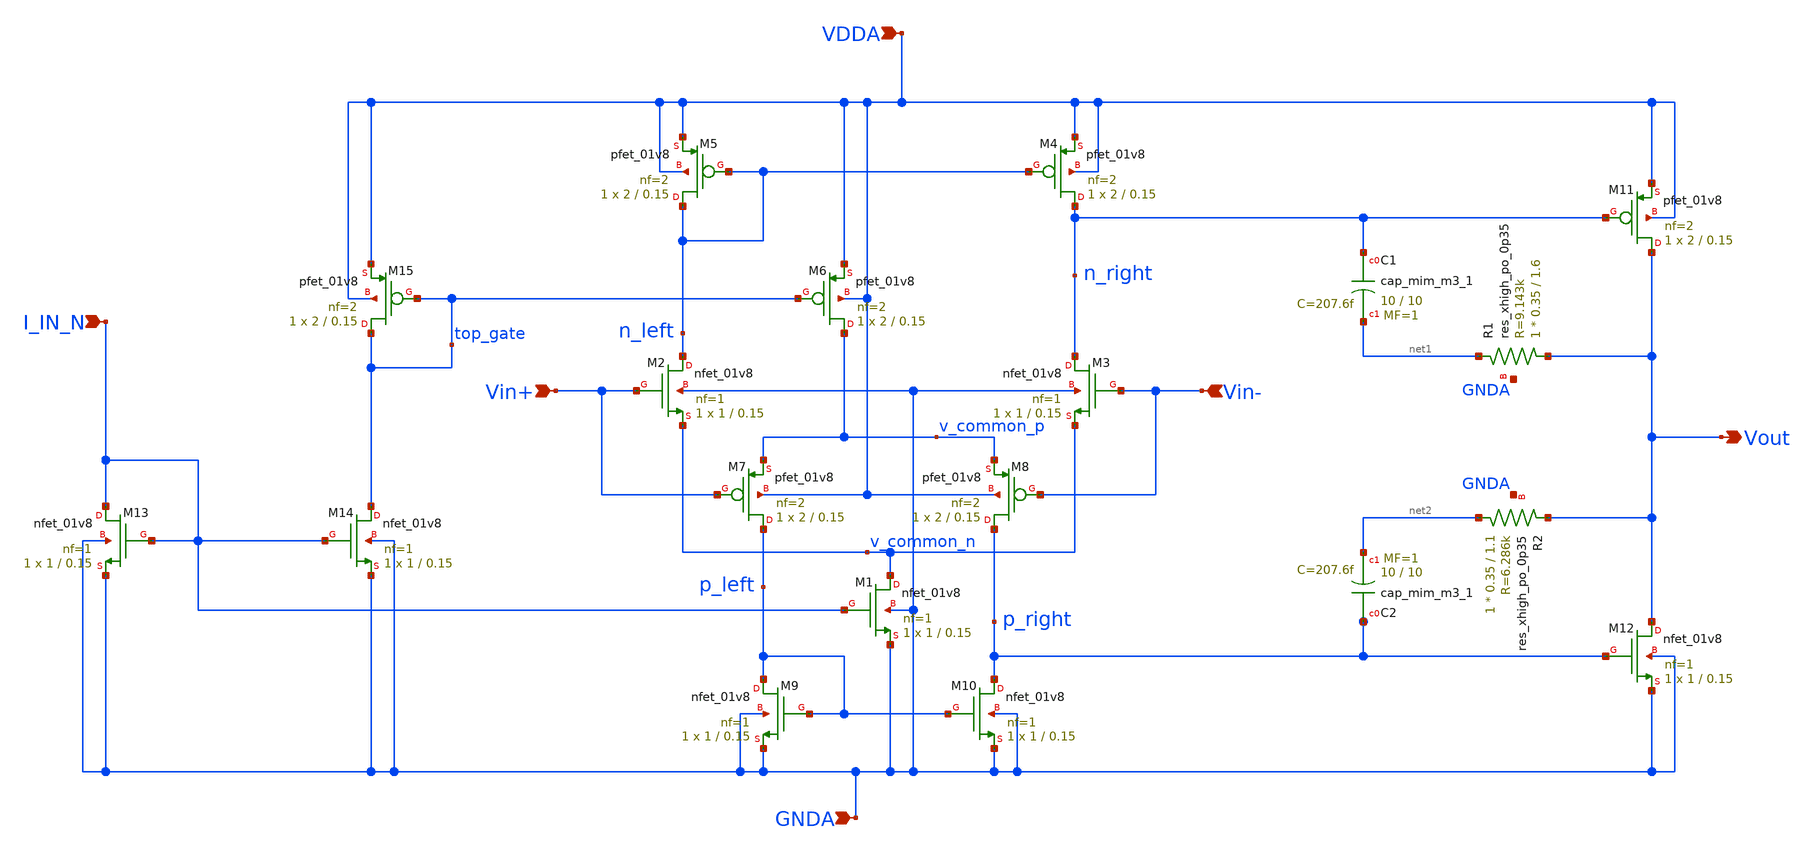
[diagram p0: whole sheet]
** sch_path: projects/pll/charge_pump/xschem_ngspice/rail_to_rail_opamp7.sch
**.subckt rail_to_rail_opamp7 Vout Vin+ Vin- VDDA GNDA I_IN_N
*.opin Vout
*.ipin Vin+
*.ipin Vin-
*.ipin VDDA
*.ipin GNDA
*.ipin I_IN_N
XM2 n_left Vin+ v_common_n GNDA sky130_fd_pr__nfet_01v8 L=0.15 W=1 nf=1 ad='int((nf+1)/2) * W/nf * 0.29'
+ as='int((nf+2)/2) * W/nf * 0.29' pd='2*int((nf+1)/2) * (W/nf + 0.29)' ps='2*int((nf+2)/2) * (W/nf + 0.29)'
+ nrd='0.29 / W' nrs='0.29 / W' sa=0 sb=0 sd=0 mult=1 m=1
XM3 n_right Vin- v_common_n GNDA sky130_fd_pr__nfet_01v8 L=0.15 W=1 nf=1 ad='int((nf+1)/2) * W/nf * 0.29'
+ as='int((nf+2)/2) * W/nf * 0.29' pd='2*int((nf+1)/2) * (W/nf + 0.29)' ps='2*int((nf+2)/2) * (W/nf + 0.29)'
+ nrd='0.29 / W' nrs='0.29 / W' sa=0 sb=0 sd=0 mult=1 m=1
XM5 n_left n_left VDDA VDDA sky130_fd_pr__pfet_01v8 L=0.15 W=2 nf=2 ad='int((nf+1)/2) * W/nf * 0.29'
+ as='int((nf+2)/2) * W/nf * 0.29' pd='2*int((nf+1)/2) * (W/nf + 0.29)' ps='2*int((nf+2)/2) * (W/nf + 0.29)'
+ nrd='0.29 / W' nrs='0.29 / W' sa=0 sb=0 sd=0 mult=1 m=1
XM4 n_right n_left VDDA VDDA sky130_fd_pr__pfet_01v8 L=0.15 W=2 nf=2 ad='int((nf+1)/2) * W/nf * 0.29'
+ as='int((nf+2)/2) * W/nf * 0.29' pd='2*int((nf+1)/2) * (W/nf + 0.29)' ps='2*int((nf+2)/2) * (W/nf + 0.29)'
+ nrd='0.29 / W' nrs='0.29 / W' sa=0 sb=0 sd=0 mult=1 m=1
XM6 v_common_p top_gate VDDA VDDA sky130_fd_pr__pfet_01v8 L=0.15 W=2 nf=2 ad='int((nf+1)/2) * W/nf * 0.29'
+ as='int((nf+2)/2) * W/nf * 0.29' pd='2*int((nf+1)/2) * (W/nf + 0.29)' ps='2*int((nf+2)/2) * (W/nf + 0.29)'
+ nrd='0.29 / W' nrs='0.29 / W' sa=0 sb=0 sd=0 mult=1 m=1
XM7 p_left Vin+ v_common_p VDDA sky130_fd_pr__pfet_01v8 L=0.15 W=2 nf=2 ad='int((nf+1)/2) * W/nf * 0.29'
+ as='int((nf+2)/2) * W/nf * 0.29' pd='2*int((nf+1)/2) * (W/nf + 0.29)' ps='2*int((nf+2)/2) * (W/nf + 0.29)'
+ nrd='0.29 / W' nrs='0.29 / W' sa=0 sb=0 sd=0 mult=1 m=1
XM8 p_right Vin- v_common_p VDDA sky130_fd_pr__pfet_01v8 L=0.15 W=2 nf=2 ad='int((nf+1)/2) * W/nf * 0.29'
+ as='int((nf+2)/2) * W/nf * 0.29' pd='2*int((nf+1)/2) * (W/nf + 0.29)' ps='2*int((nf+2)/2) * (W/nf + 0.29)'
+ nrd='0.29 / W' nrs='0.29 / W' sa=0 sb=0 sd=0 mult=1 m=1
XM9 p_left p_left GNDA GNDA sky130_fd_pr__nfet_01v8 L=0.15 W=1 nf=1 ad='int((nf+1)/2) * W/nf * 0.29'
+ as='int((nf+2)/2) * W/nf * 0.29' pd='2*int((nf+1)/2) * (W/nf + 0.29)' ps='2*int((nf+2)/2) * (W/nf + 0.29)'
+ nrd='0.29 / W' nrs='0.29 / W' sa=0 sb=0 sd=0 mult=1 m=1
XM10 p_right p_left GNDA GNDA sky130_fd_pr__nfet_01v8 L=0.15 W=1 nf=1 ad='int((nf+1)/2) * W/nf * 0.29'
+ as='int((nf+2)/2) * W/nf * 0.29' pd='2*int((nf+1)/2) * (W/nf + 0.29)' ps='2*int((nf+2)/2) * (W/nf + 0.29)'
+ nrd='0.29 / W' nrs='0.29 / W' sa=0 sb=0 sd=0 mult=1 m=1
XM1 v_common_n I_IN_N GNDA GNDA sky130_fd_pr__nfet_01v8 L=0.15 W=1 nf=1 ad='int((nf+1)/2) * W/nf * 0.29'
+ as='int((nf+2)/2) * W/nf * 0.29' pd='2*int((nf+1)/2) * (W/nf + 0.29)' ps='2*int((nf+2)/2) * (W/nf + 0.29)'
+ nrd='0.29 / W' nrs='0.29 / W' sa=0 sb=0 sd=0 mult=1 m=1
XM11 Vout n_right VDDA VDDA sky130_fd_pr__pfet_01v8 L=0.15 W=2 nf=2 ad='int((nf+1)/2) * W/nf * 0.29'
+ as='int((nf+2)/2) * W/nf * 0.29' pd='2*int((nf+1)/2) * (W/nf + 0.29)' ps='2*int((nf+2)/2) * (W/nf + 0.29)'
+ nrd='0.29 / W' nrs='0.29 / W' sa=0 sb=0 sd=0 mult=1 m=1
XM12 Vout p_right GNDA GNDA sky130_fd_pr__nfet_01v8 L=0.15 W=1 nf=1 ad='int((nf+1)/2) * W/nf * 0.29'
+ as='int((nf+2)/2) * W/nf * 0.29' pd='2*int((nf+1)/2) * (W/nf + 0.29)' ps='2*int((nf+2)/2) * (W/nf + 0.29)'
+ nrd='0.29 / W' nrs='0.29 / W' sa=0 sb=0 sd=0 mult=1 m=1
XM13 I_IN_N I_IN_N GNDA GNDA sky130_fd_pr__nfet_01v8 L=0.15 W=1 nf=1 ad='int((nf+1)/2) * W/nf * 0.29'
+ as='int((nf+2)/2) * W/nf * 0.29' pd='2*int((nf+1)/2) * (W/nf + 0.29)' ps='2*int((nf+2)/2) * (W/nf + 0.29)'
+ nrd='0.29 / W' nrs='0.29 / W' sa=0 sb=0 sd=0 mult=1 m=1
XM15 top_gate top_gate VDDA VDDA sky130_fd_pr__pfet_01v8 L=0.15 W=2 nf=2 ad='int((nf+1)/2) * W/nf * 0.29'
+ as='int((nf+2)/2) * W/nf * 0.29' pd='2*int((nf+1)/2) * (W/nf + 0.29)' ps='2*int((nf+2)/2) * (W/nf + 0.29)'
+ nrd='0.29 / W' nrs='0.29 / W' sa=0 sb=0 sd=0 mult=1 m=1
XM14 top_gate I_IN_N GNDA GNDA sky130_fd_pr__nfet_01v8 L=0.15 W=1 nf=1 ad='int((nf+1)/2) * W/nf * 0.29'
+ as='int((nf+2)/2) * W/nf * 0.29' pd='2*int((nf+1)/2) * (W/nf + 0.29)' ps='2*int((nf+2)/2) * (W/nf + 0.29)'
+ nrd='0.29 / W' nrs='0.29 / W' sa=0 sb=0 sd=0 mult=1 m=1
XC1 n_right net1 sky130_fd_pr__cap_mim_m3_1 W=10 L=10 MF=1 m=1
XC2 p_right net2 sky130_fd_pr__cap_mim_m3_1 W=10 L=10 MF=1 m=1
XR1 Vout net1 GNDA sky130_fd_pr__res_xhigh_po_0p35 L=1.6 mult=1 m=1
XR2 net2 Vout GNDA sky130_fd_pr__res_xhigh_po_0p35 L=1.1 mult=1 m=1
**.ends
.end
